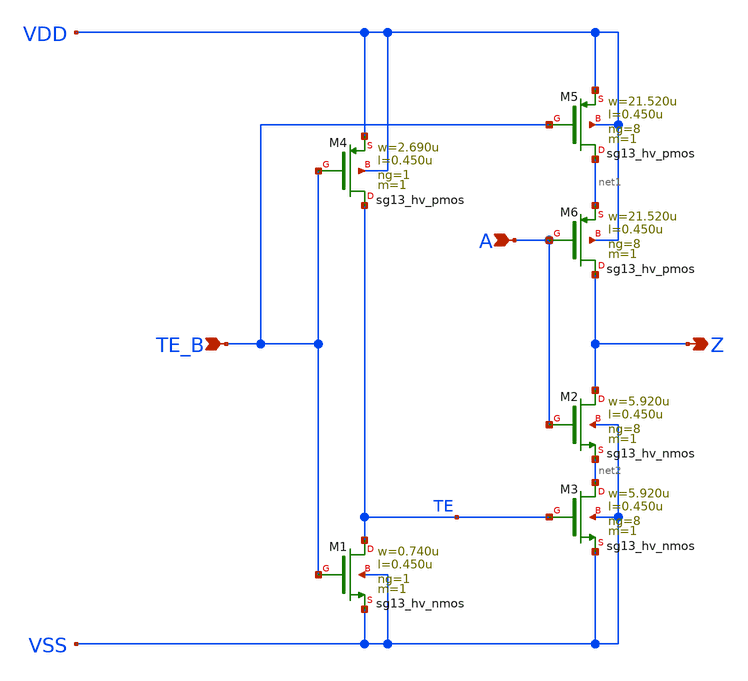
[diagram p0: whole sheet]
** sch_path: ihp-sg13g2/libs.ref/sg13g2_stdcell_hv/sch/xschem/sg13g2_hv_einvn_8.sch
* Copyright 2023 IHP PDK Authors
* Licensed under the Apache License, Version 2.0 (the "License");
* you may not use this file except in compliance with the License.
* You may obtain a copy of the License at
* https://www.apache.org/licenses/LICENSE-2.0
* Unless required by applicable law or agreed to in writing, software
* distributed under the License is distributed on an "AS IS" BASIS,
* WITHOUT WARRANTIES OR CONDITIONS OF ANY KIND, either express or implied.
* See the License for the specific language governing permissions and
* limitations under the License.
**.subckt sg13g2_hv_einvn_8 TE_B A Z
*.ipin TE_B
*.ipin A
*.opin Z
XM1 TE TE_B VSS VSS sg13_hv_nmos w=0.740u l=0.450u ng=1 m=1 mm_ok=1
XM2 Z A net2 VSS sg13_hv_nmos w=5.920u l=0.450u ng=8 m=1 mm_ok=1
XM3 net2 TE VSS VSS sg13_hv_nmos w=5.920u l=0.450u ng=8 m=1 mm_ok=1
XM4 TE TE_B VDD VDD sg13_hv_pmos w=2.690u l=0.450u ng=1 m=1 mm_ok=1
XM5 net1 TE_B VDD VDD sg13_hv_pmos w=21.520u l=0.450u ng=8 m=1 mm_ok=1
XM6 Z A net1 VDD sg13_hv_pmos w=21.520u l=0.450u ng=8 m=1 mm_ok=1
**.ends
.end
